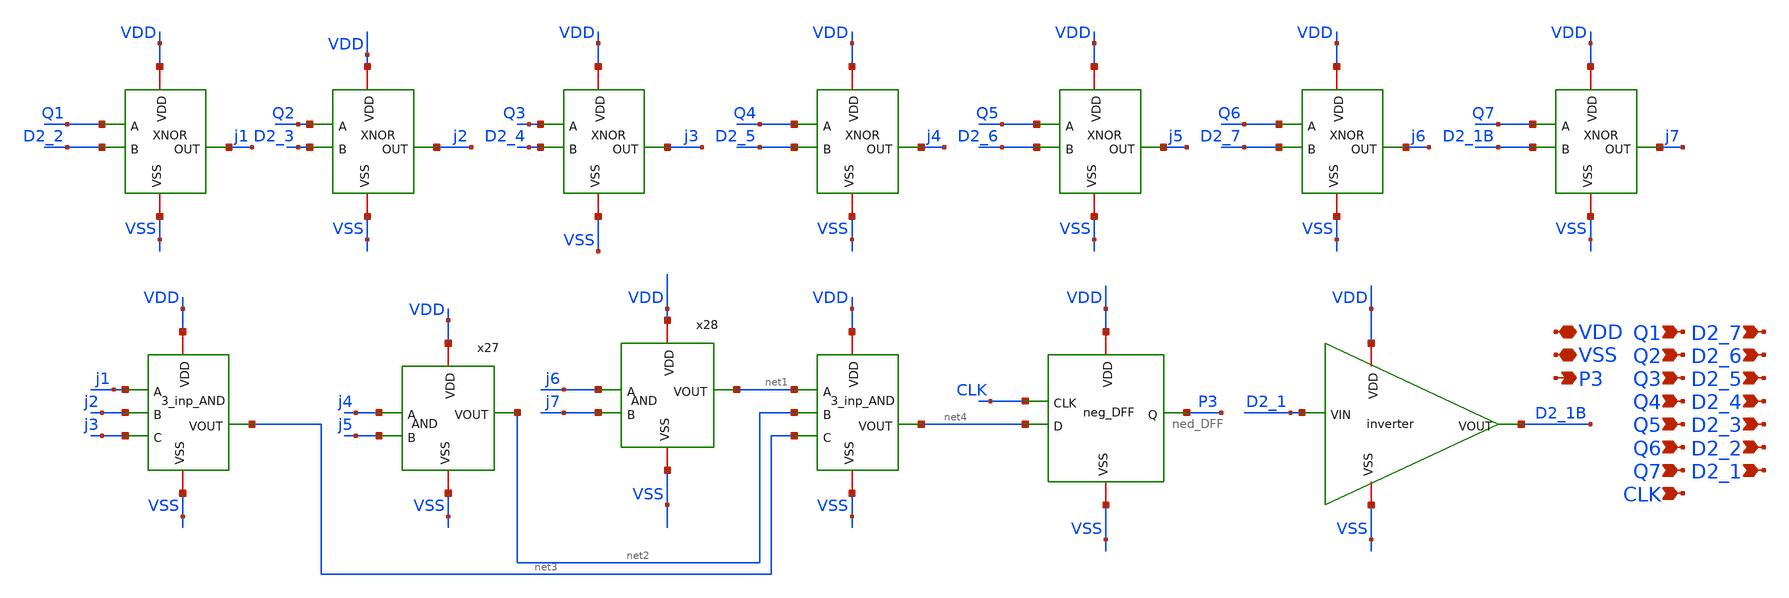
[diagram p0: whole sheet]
** sch_path: Xschem/PLL_TOP_Schematics/P3_GENERATION.sch
**.subckt P3_GENERATION VDD VSS Q1 Q2 Q3 Q4 Q5 Q6 Q7 D2_1 D2_2 D2_3 D2_4 D2_5 D2_6 D2_7 CLK P3
*.iopin VDD
*.iopin VSS
*.ipin Q1
*.ipin Q2
*.ipin Q3
*.ipin Q4
*.ipin Q5
*.ipin Q6
*.ipin Q7
*.ipin D2_1
*.ipin D2_2
*.ipin D2_3
*.ipin D2_4
*.ipin D2_5
*.ipin D2_6
*.ipin D2_7
*.ipin CLK
*.opin P3
x14 VDD Q2 j2 D2_3 VSS XNOR
x18 VDD Q1 j1 D2_2 VSS XNOR
x19 VDD Q3 j3 D2_4 VSS XNOR
x20 VDD Q4 j4 D2_5 VSS XNOR
x21 VDD Q5 j5 D2_6 VSS XNOR
x22 VDD Q6 j6 D2_7 VSS XNOR
x23 VDD Q7 j7 D2_1B VSS XNOR
x24 VDD D2_1 D2_1B VSS inverter
x25 VDD net3 j1 j2 j3 VSS 3_inp_AND
x26 VDD net4 net1 net2 net3 VSS 3_inp_AND
x27 VDD net2 j4 j5 VSS AND
x28 VDD net1 j6 j7 VSS AND
x29 CLK VDD net4 P3 VSS ned_DFF
**.ends
.end
